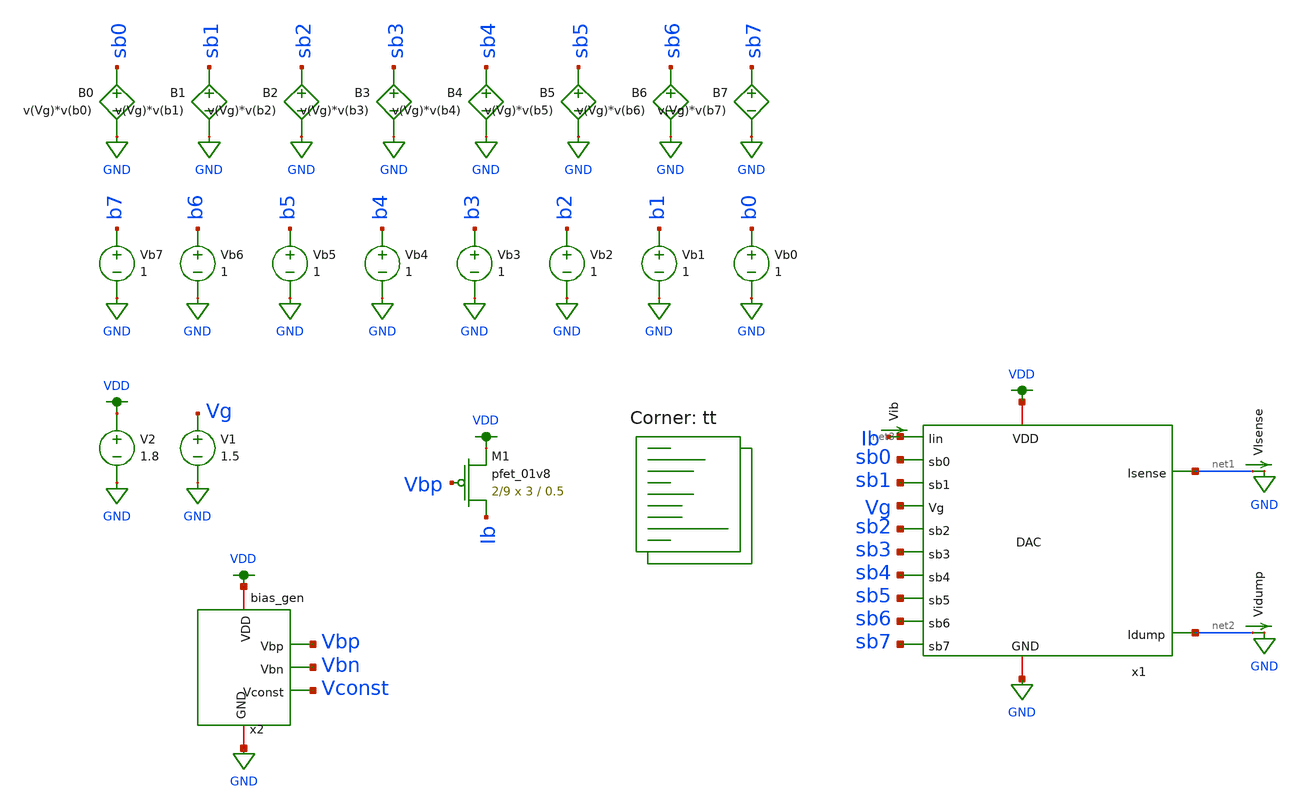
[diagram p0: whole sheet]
** sch_path: final/schematics/dac_tb.sch
**.subckt dac_tb
x1 sb0 VDD GND sb1 Vg sb2 sb3 net1 sb4 net2 sb5 sb6 sb7 net3 dac
Vb0 b0 GND 1
B0 sb0 GND V=v(Vg)*v(b0)
Vb1 b1 GND 1
B1 sb1 GND V=v(Vg)*v(b1)
Vb2 b2 GND 1
B2 sb2 GND V=v(Vg)*v(b2)
Vb3 b3 GND 1
B3 sb3 GND V=v(Vg)*v(b3)
Vb4 b4 GND 1
B4 sb4 GND V=v(Vg)*v(b4)
Vb5 b5 GND 1
B5 sb5 GND V=v(Vg)*v(b5)
Vb6 b6 GND 1
B6 sb6 GND V=v(Vg)*v(b6)
VIsense net1 GND 0
.save i(visense)
Vidump net2 GND 0
.save i(vidump)
Vb7 b7 GND 1
B7 sb7 GND V=v(Vg)*v(b7)
V2 VDD GND 1.8
V1 Vg GND 1.5
x2 VDD Vbp Vconst GND Vbn bias_gen
XM1 Ib Vbp VDD VDD sky130_fd_pr__pfet_01v8 L=0.5 W=3 nf=1 ad='int((nf+1)/2) * W/nf * 0.29' as='int((nf+2)/2) * W/nf * 0.29'
+ pd='2*int((nf+1)/2) * (W/nf + 0.29)' ps='2*int((nf+2)/2) * (W/nf + 0.29)' nrd='0.29 / W' nrs='0.29 / W'
+ sa=0 sb=0 sd=0 mult=2/9 m=2/9
Vib Ib net3 0
.save i(vib)
**** begin user architecture code
.lib $::SKYWATER_MODELS/sky130.lib.spice tt


.control
  let mc_runs = 1
  let run = 1
  dowhile run <= mc_runs
    set wr_vecnames
    set appendwrite = FALSE
    set wr_singlescale
    let code = 0
    while code < 256
      if code eq 0
        let b0 = 0
      else
        let b0 = code % 2
      end
      if floor(code / 2) eq 0
        let b1 = 0
      else
        let b1 = floor(code / 2) % 2
      end
      if floor(code / 4) eq 0
        let b2 = 0
      else
        let b2 = floor(code / 4) % 2
      end
      if floor(code / 8) eq 0
        let b3 = 0
      else
        let b3 = floor(code / 8) % 2
      end
      if floor(code / 16) eq 0
        let b4 = 0
      else
        let b4 = floor(code / 16) % 2
      end
      if floor(code / 32) eq 0
        let b5 = 0
      else
        let b5 = floor(code / 32) % 2
      end
      if floor(code / 64) eq 0
        let b6 = 0
      else
        let b6 = floor(code / 64) % 2
      end
      if floor(code / 128) eq 0
        let b7 = 0
      else
        let b7 = floor(code / 128) % 2
      end
      alter vb0 $&b0
      alter vb1 $&b1
      alter vb2 $&b2
      alter vb3 $&b3
      alter vb4 $&b4
      alter vb5 $&b5
      alter vb6 $&b6
      alter vb7 $&b7
      save all
      op
      wrdata ~/Documents/madvlsi/final/schematics/dactest/dac_tb{$&run}.txt code v(sb0) v(sb1) v(sb2)
+ v(sb3) v(sb4) v(sb5) v(sb6) v(sb7) v(vconst) i(vib) i(visense) i(vidump)
      if code eq 0
        set appendwrite
        set wr_vecnames = FALSE
      end
      let code = code + 1
    end
    reset
    let run = run + 1
  end
quit
.endc

**** end user architecture code
**.ends
.GLOBAL GND
.GLOBAL VDD
.end
